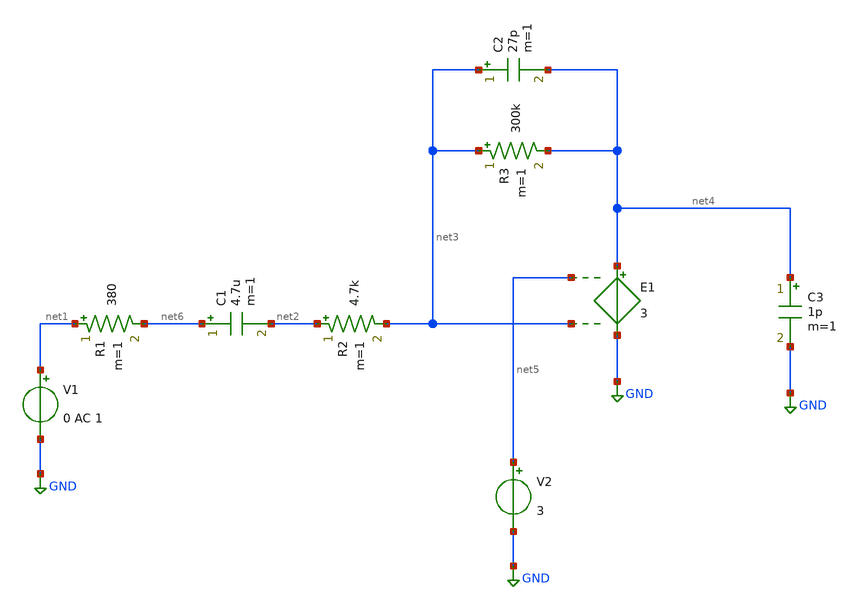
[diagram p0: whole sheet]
** sch_path: xschem/untitled.sch
**.subckt untitled
V1 net1 GND 0 AC 1
R1 net1 net6 380 m=1
C1 net6 net2 4.7u m=1
R2 net2 net3 4.7k m=1
E1 net4 GND net5 net3 3
R3 net3 net4 300k m=1
C2 net3 net4 27p m=1
V2 net5 GND 3
C3 net4 GND 1p m=1
**.ends
.GLOBAL GND
.end
